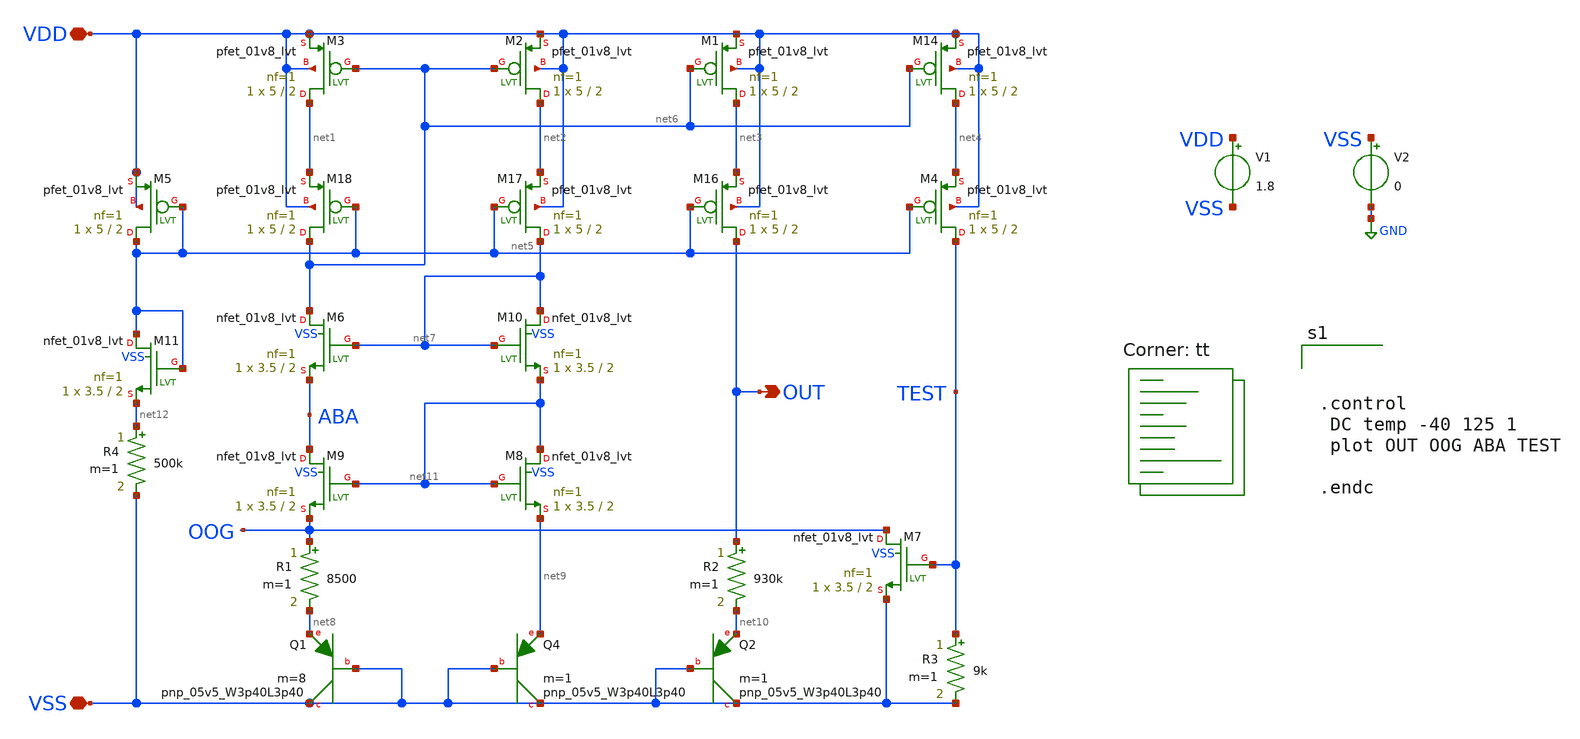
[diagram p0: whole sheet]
** sch_path: bandgap/bgr.sch
**.subckt bgr VDD VSS OUT
*.iopin VDD
*.iopin VSS
*.opin OUT
V1 VDD VSS 1.8
V2 VSS GND 0
R1 OOG net8 8500 m=1
R2 OUT net10 930k m=1
R3 TEST VSS 9k m=1
XQ4 VSS VSS net9 sky130_fd_pr__pnp_05v5_W3p40L3p40 m=1
XQ1 VSS VSS net8 sky130_fd_pr__pnp_05v5_W3p40L3p40 m=8
XQ2 VSS VSS net10 sky130_fd_pr__pnp_05v5_W3p40L3p40 m=1
XM14 net4 net6 VDD VDD sky130_fd_pr__pfet_01v8_lvt L=2 W=5 nf=1 ad='int((nf+1)/2) * W/nf * 0.29' as='int((nf+2)/2) * W/nf * 0.29'
+ pd='2*int((nf+1)/2) * (W/nf + 0.29)' ps='2*int((nf+2)/2) * (W/nf + 0.29)' nrd='0.29 / W' nrs='0.29 / W'
+ sa=0 sb=0 sd=0 mult=1 m=1
XM1 net3 net6 VDD VDD sky130_fd_pr__pfet_01v8_lvt L=2 W=5 nf=1 ad='int((nf+1)/2) * W/nf * 0.29' as='int((nf+2)/2) * W/nf * 0.29'
+ pd='2*int((nf+1)/2) * (W/nf + 0.29)' ps='2*int((nf+2)/2) * (W/nf + 0.29)' nrd='0.29 / W' nrs='0.29 / W'
+ sa=0 sb=0 sd=0 mult=1 m=1
XM2 net2 net6 VDD VDD sky130_fd_pr__pfet_01v8_lvt L=2 W=5 nf=1 ad='int((nf+1)/2) * W/nf * 0.29' as='int((nf+2)/2) * W/nf * 0.29'
+ pd='2*int((nf+1)/2) * (W/nf + 0.29)' ps='2*int((nf+2)/2) * (W/nf + 0.29)' nrd='0.29 / W' nrs='0.29 / W'
+ sa=0 sb=0 sd=0 mult=1 m=1
XM3 net1 net6 VDD VDD sky130_fd_pr__pfet_01v8_lvt L=2 W=5 nf=1 ad='int((nf+1)/2) * W/nf * 0.29' as='int((nf+2)/2) * W/nf * 0.29'
+ pd='2*int((nf+1)/2) * (W/nf + 0.29)' ps='2*int((nf+2)/2) * (W/nf + 0.29)' nrd='0.29 / W' nrs='0.29 / W'
+ sa=0 sb=0 sd=0 mult=1 m=1
XM4 TEST net5 net4 VDD sky130_fd_pr__pfet_01v8_lvt L=2 W=5 nf=1 ad='int((nf+1)/2) * W/nf * 0.29' as='int((nf+2)/2) * W/nf * 0.29'
+ pd='2*int((nf+1)/2) * (W/nf + 0.29)' ps='2*int((nf+2)/2) * (W/nf + 0.29)' nrd='0.29 / W' nrs='0.29 / W'
+ sa=0 sb=0 sd=0 mult=1 m=1
XM16 OUT net5 net3 VDD sky130_fd_pr__pfet_01v8_lvt L=2 W=5 nf=1 ad='int((nf+1)/2) * W/nf * 0.29' as='int((nf+2)/2) * W/nf * 0.29'
+ pd='2*int((nf+1)/2) * (W/nf + 0.29)' ps='2*int((nf+2)/2) * (W/nf + 0.29)' nrd='0.29 / W' nrs='0.29 / W'
+ sa=0 sb=0 sd=0 mult=1 m=1
XM17 net7 net5 net2 VDD sky130_fd_pr__pfet_01v8_lvt L=2 W=5 nf=1 ad='int((nf+1)/2) * W/nf * 0.29' as='int((nf+2)/2) * W/nf * 0.29'
+ pd='2*int((nf+1)/2) * (W/nf + 0.29)' ps='2*int((nf+2)/2) * (W/nf + 0.29)' nrd='0.29 / W' nrs='0.29 / W'
+ sa=0 sb=0 sd=0 mult=1 m=1
XM18 net6 net5 net1 VDD sky130_fd_pr__pfet_01v8_lvt L=2 W=5 nf=1 ad='int((nf+1)/2) * W/nf * 0.29' as='int((nf+2)/2) * W/nf * 0.29'
+ pd='2*int((nf+1)/2) * (W/nf + 0.29)' ps='2*int((nf+2)/2) * (W/nf + 0.29)' nrd='0.29 / W' nrs='0.29 / W'
+ sa=0 sb=0 sd=0 mult=1 m=1
XM5 net5 net5 VDD VDD sky130_fd_pr__pfet_01v8_lvt L=2 W=5 nf=1 ad='int((nf+1)/2) * W/nf * 0.29' as='int((nf+2)/2) * W/nf * 0.29'
+ pd='2*int((nf+1)/2) * (W/nf + 0.29)' ps='2*int((nf+2)/2) * (W/nf + 0.29)' nrd='0.29 / W' nrs='0.29 / W'
+ sa=0 sb=0 sd=0 mult=1 m=1
XM10 net7 net7 net11 VSS sky130_fd_pr__nfet_01v8_lvt L=2 W=3.5 nf=1 ad='int((nf+1)/2) * W/nf * 0.29'
+ as='int((nf+2)/2) * W/nf * 0.29' pd='2*int((nf+1)/2) * (W/nf + 0.29)' ps='2*int((nf+2)/2) * (W/nf + 0.29)'
+ nrd='0.29 / W' nrs='0.29 / W' sa=0 sb=0 sd=0 mult=1 m=1
XM6 net6 net7 ABA VSS sky130_fd_pr__nfet_01v8_lvt L=2 W=3.5 nf=1 ad='int((nf+1)/2) * W/nf * 0.29' as='int((nf+2)/2) * W/nf * 0.29'
+ pd='2*int((nf+1)/2) * (W/nf + 0.29)' ps='2*int((nf+2)/2) * (W/nf + 0.29)' nrd='0.29 / W' nrs='0.29 / W'
+ sa=0 sb=0 sd=0 mult=1 m=1
XM7 OOG TEST VSS VSS sky130_fd_pr__nfet_01v8_lvt L=2 W=3.5 nf=1 ad='int((nf+1)/2) * W/nf * 0.29' as='int((nf+2)/2) * W/nf * 0.29'
+ pd='2*int((nf+1)/2) * (W/nf + 0.29)' ps='2*int((nf+2)/2) * (W/nf + 0.29)' nrd='0.29 / W' nrs='0.29 / W'
+ sa=0 sb=0 sd=0 mult=1 m=1
XM8 net11 net11 net9 VSS sky130_fd_pr__nfet_01v8_lvt L=2 W=3.5 nf=1 ad='int((nf+1)/2) * W/nf * 0.29'
+ as='int((nf+2)/2) * W/nf * 0.29' pd='2*int((nf+1)/2) * (W/nf + 0.29)' ps='2*int((nf+2)/2) * (W/nf + 0.29)'
+ nrd='0.29 / W' nrs='0.29 / W' sa=0 sb=0 sd=0 mult=1 m=1
XM9 ABA net11 OOG VSS sky130_fd_pr__nfet_01v8_lvt L=2 W=3.5 nf=1 ad='int((nf+1)/2) * W/nf * 0.29' as='int((nf+2)/2) * W/nf * 0.29'
+ pd='2*int((nf+1)/2) * (W/nf + 0.29)' ps='2*int((nf+2)/2) * (W/nf + 0.29)' nrd='0.29 / W' nrs='0.29 / W'
+ sa=0 sb=0 sd=0 mult=1 m=1
R4 net12 VSS 500k m=1
XM11 net5 net5 net12 VSS sky130_fd_pr__nfet_01v8_lvt L=2 W=3.5 nf=1 ad='int((nf+1)/2) * W/nf * 0.29'
+ as='int((nf+2)/2) * W/nf * 0.29' pd='2*int((nf+1)/2) * (W/nf + 0.29)' ps='2*int((nf+2)/2) * (W/nf + 0.29)'
+ nrd='0.29 / W' nrs='0.29 / W' sa=0 sb=0 sd=0 mult=1 m=1
**** begin user architecture code
.lib $::SKYWATER_MODELS/sky130.lib.spice tt



.control
 DC temp -40 125 1
 plot OUT OOG ABA TEST

.endc


**** end user architecture code
**.ends
.GLOBAL GND
.end
